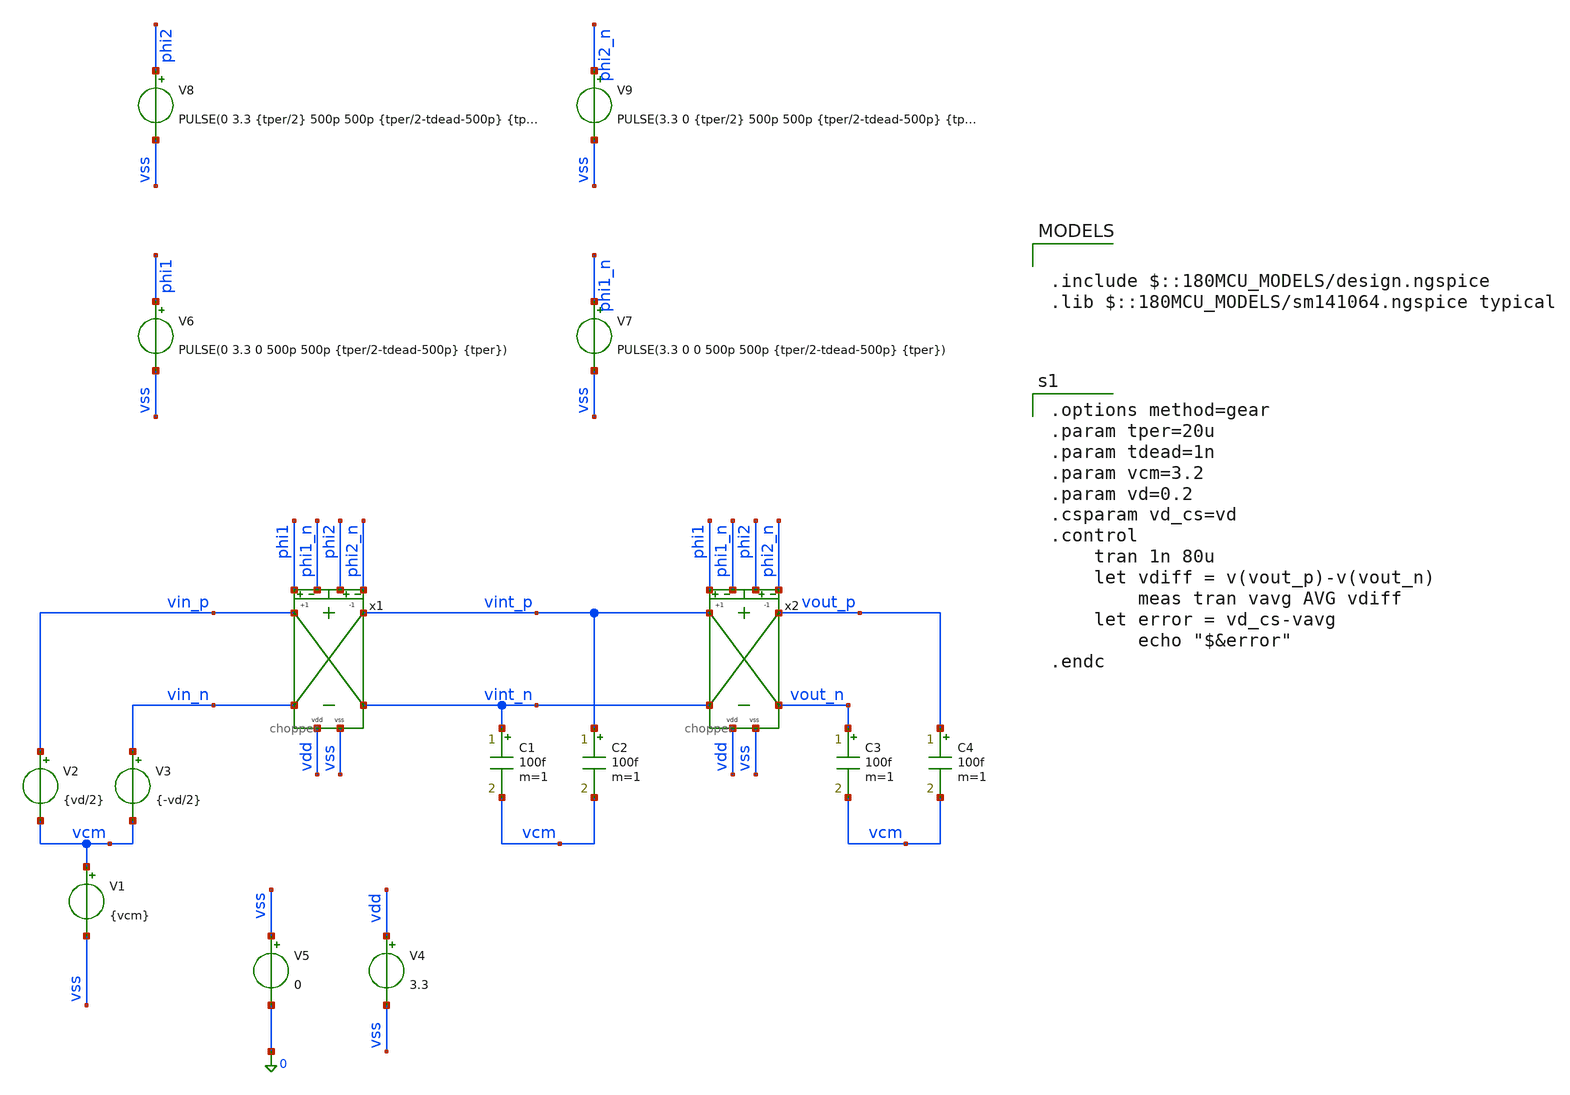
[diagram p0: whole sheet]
** sch_path: xschem/archive/chopper/chopper_tb.sch
**.subckt chopper_tb
x1 phi1 vss vin_p phi2 vin_n phi1_n phi2_n vint_p vint_n vdd chopper
V1 vcm vss {vcm}
V2 vin_p vcm {vd/2}
V3 vin_n vcm {-vd/2}
C1 vint_n vcm 100f m=1
C2 vint_p vcm 100f m=1
V4 vdd vss 3.3
V5 vss 0 0
V6 phi1 vss PULSE(0 3.3 0 500p 500p {tper/2-tdead-500p} {tper})
V7 phi1_n vss PULSE(3.3 0 0 500p 500p {tper/2-tdead-500p} {tper})
V8 phi2 vss PULSE(0 3.3 {tper/2} 500p 500p {tper/2-tdead-500p} {tper})
V9 phi2_n vss PULSE(3.3 0 {tper/2} 500p 500p {tper/2-tdead-500p} {tper})
x2 phi1 vss vint_p phi2 vint_n phi1_n phi2_n vout_p vout_n vdd chopper
C3 vout_n vcm 100f m=1
C4 vout_p vcm 100f m=1
**** begin user architecture code

.include $::180MCU_MODELS/design.ngspice
.lib $::180MCU_MODELS/sm141064.ngspice typical


.options method=gear
.param tper=20u
.param tdead=1n
.param vcm=3.2
.param vd=0.2
.csparam vd_cs=vd
.control
	tran 1n 80u
	let vdiff = v(vout_p)-v(vout_n)
        meas tran vavg AVG vdiff
	let error = vd_cs-vavg
        echo "$&error"
.endc

**** end user architecture code
**.ends
.end
